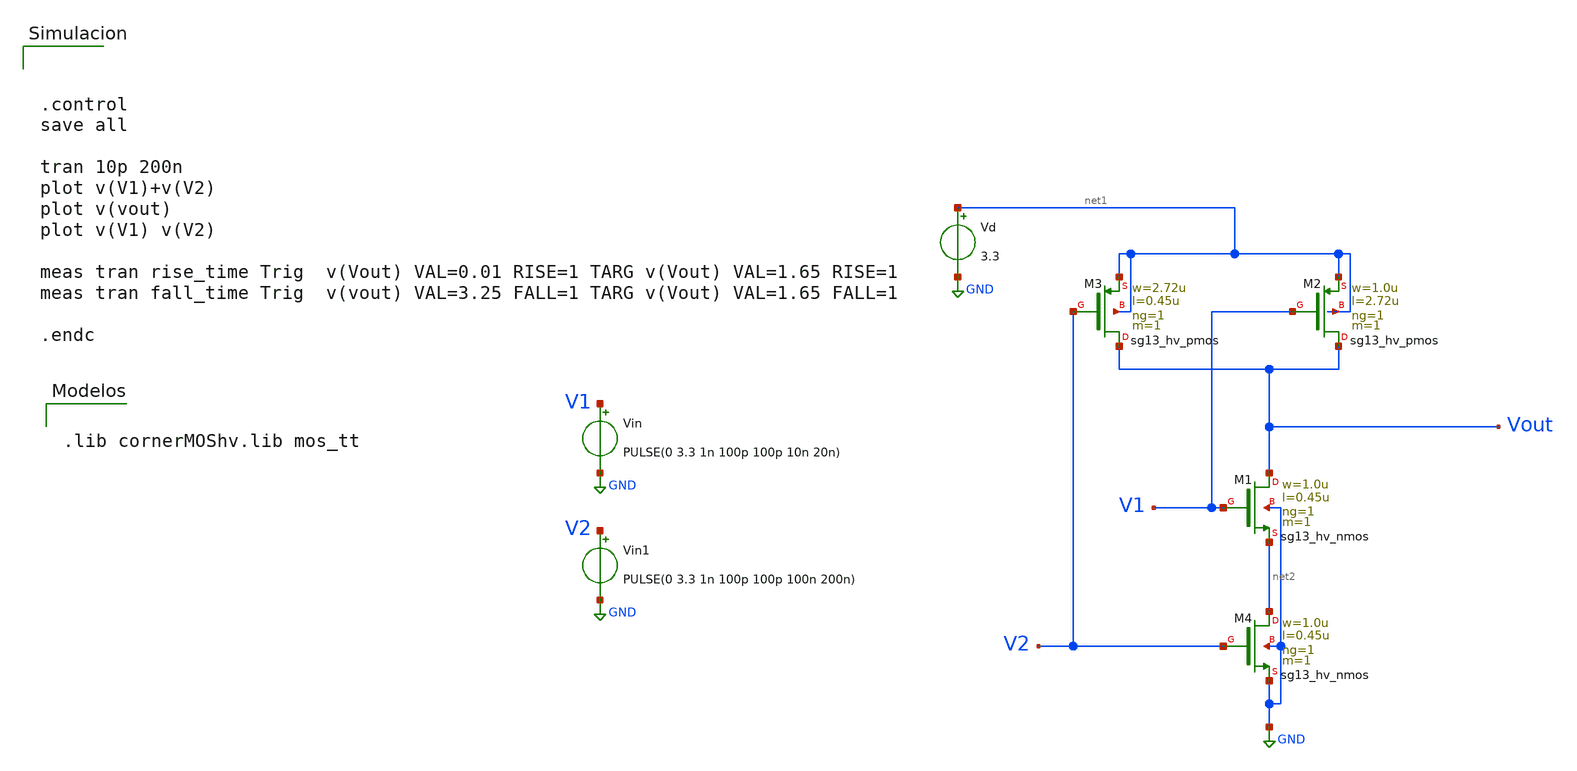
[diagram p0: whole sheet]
** sch_path: Taller2/Resuelto/nand_sim.sch
**.subckt nand_sim
XM1 Vout V1 net2 GND sg13_hv_nmos w=1.0u l=0.45u ng=1 m=1 mm_ok=1
XM2 Vout V1 net1 net1 sg13_hv_pmos w=1.0u l=2.72u ng=1 m=1 mm_ok=1
XM3 Vout V2 net1 net1 sg13_hv_pmos w=2.72u l=0.45u ng=1 m=1 mm_ok=1
XM4 net2 V2 GND GND sg13_hv_nmos w=1.0u l=0.45u ng=1 m=1 mm_ok=1
Vd net1 GND 3.3
Vin V1 GND PULSE(0 3.3 1n 100p 100p 10n 20n)
Vin1 V2 GND PULSE(0 3.3 1n 100p 100p 100n 200n)
**** begin user architecture code



.control
save all

tran 10p 200n
plot v(V1)+v(V2)
plot v(vout)
plot v(V1) v(V2)

meas tran rise_time Trig  v(Vout) VAL=0.01 RISE=1 TARG v(Vout) VAL=1.65 RISE=1
meas tran fall_time Trig  v(vout) VAL=3.25 FALL=1 TARG v(Vout) VAL=1.65 FALL=1

.endc




.lib cornerMOShv.lib mos_tt


**** end user architecture code
**.ends
.GLOBAL GND
.end
